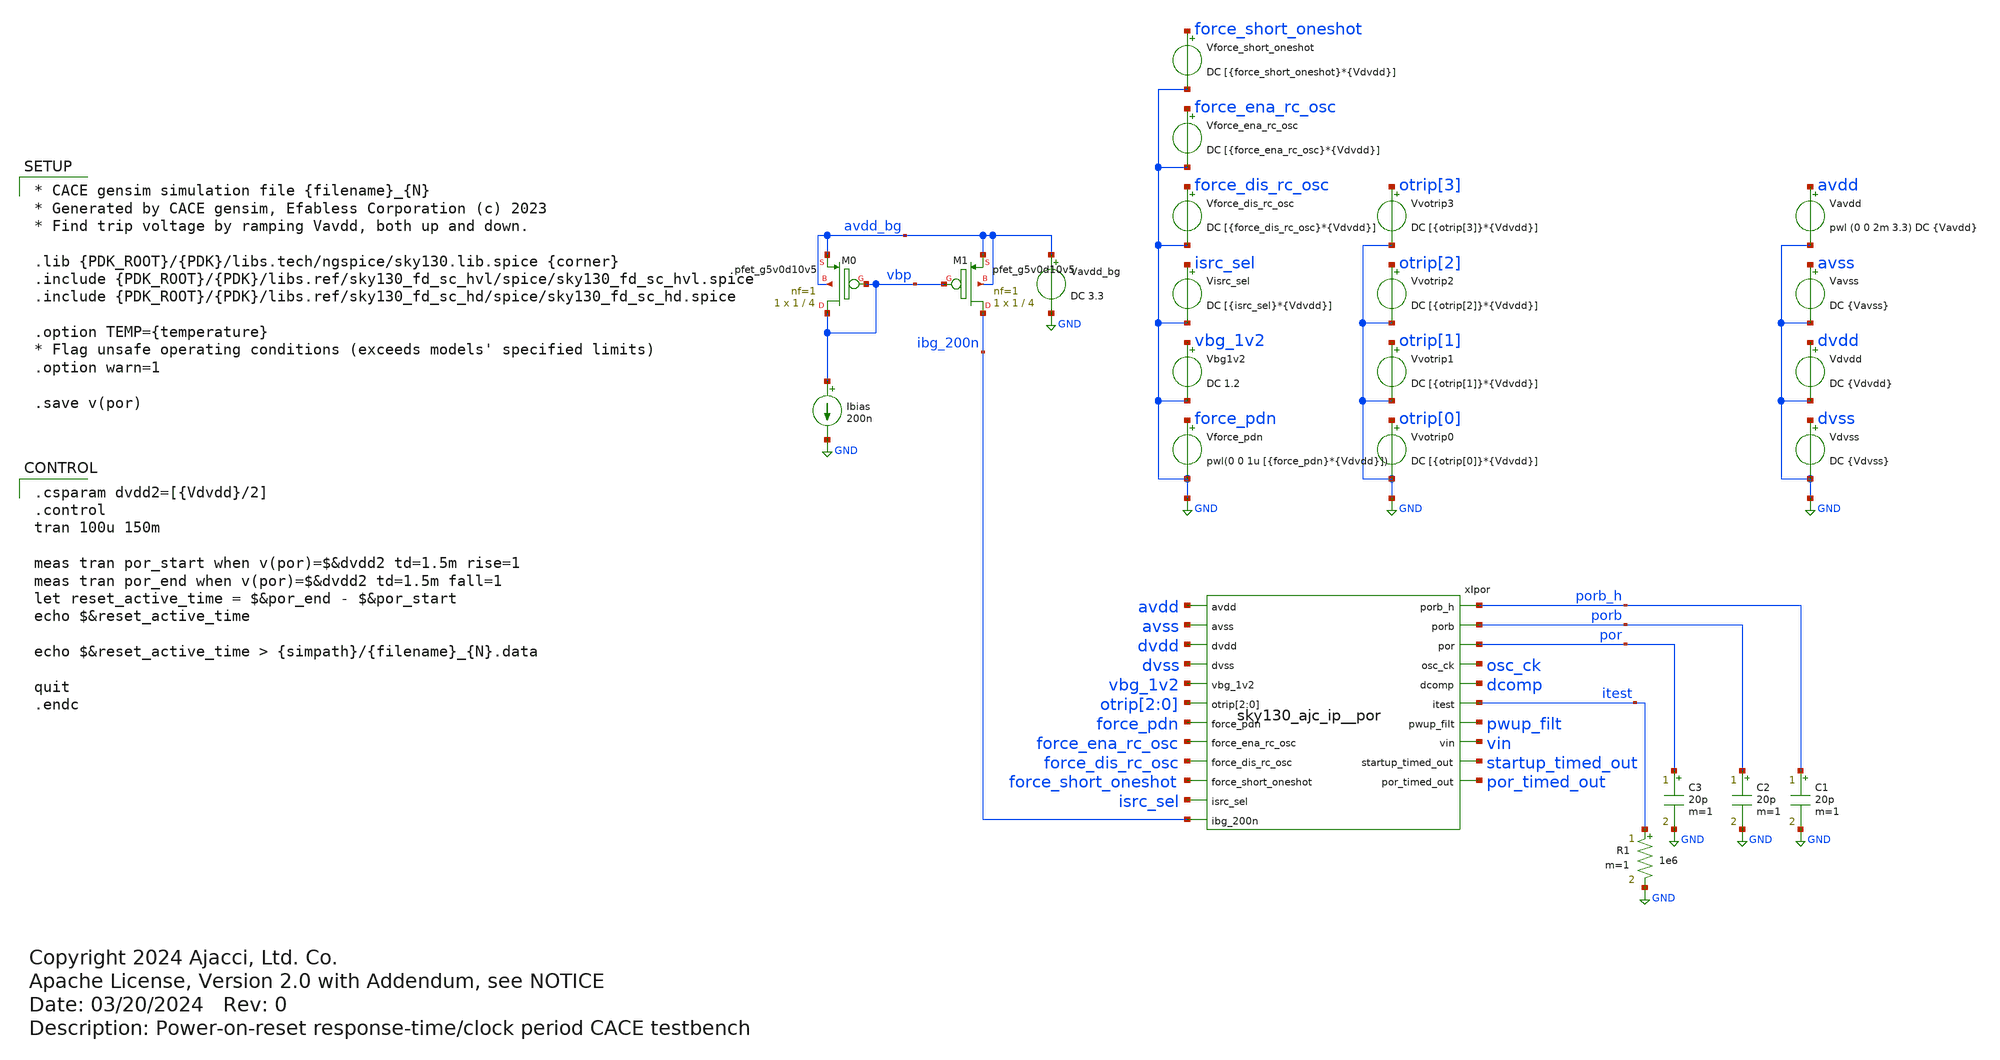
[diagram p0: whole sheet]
** sch_path: cace/transient_long.sch
* Copyright 2024 Ajacci, Ltd. Co.
* Apache License, Version 2.0 with Addendum, see NOTICE
**.subckt transient_long
Ibias vbp GND 200n
XM1 ibg_200n vbp avdd_bg avdd_bg sky130_fd_pr__pfet_g5v0d10v5 L=4 W=1 nf=1 ad='int((nf+1)/2) * W/nf * 0.29'
+ as='int((nf+2)/2) * W/nf * 0.29' pd='2*int((nf+1)/2) * (W/nf + 0.29)' ps='2*int((nf+2)/2) * (W/nf + 0.29)'
+ nrd='0.29 / W' nrs='0.29 / W' sa=0 sb=0 sd=0 mult=1 m=1
XM0 vbp vbp avdd_bg avdd_bg sky130_fd_pr__pfet_g5v0d10v5 L=4 W=1 nf=1 ad='int((nf+1)/2) * W/nf * 0.29'
+ as='int((nf+2)/2) * W/nf * 0.29' pd='2*int((nf+1)/2) * (W/nf + 0.29)' ps='2*int((nf+2)/2) * (W/nf + 0.29)'
+ nrd='0.29 / W' nrs='0.29 / W' sa=0 sb=0 sd=0 mult=1 m=1
R1 itest GND 1e6 m=1
Vavss avss GND DC {Vavss}
Vforce_pdn force_pdn GND pwl(0 0 1u [{force_pdn}*{Vdvdd}])
Vavdd avdd GND pwl (0 0 2m 3.3) DC {Vavdd}
.save i(vavdd)
Vbg1v2 vbg_1v2 GND DC 1.2
Vdvss dvss GND DC {Vdvss}
Vdvdd dvdd GND DC {Vdvdd}
.save i(vdvdd)
Vvotrip0 otrip[0] GND DC [{otrip[0]}*{Vdvdd}]
.save i(vvotrip0)
Vvotrip1 otrip[1] GND DC [{otrip[1]}*{Vdvdd}]
.save i(vvotrip1)
Vvotrip2 otrip[2] GND DC [{otrip[2]}*{Vdvdd}]
.save i(vvotrip2)
Vvotrip3 otrip[3] GND DC [{otrip[3]}*{Vdvdd}]
.save i(vvotrip3)
Visrc_sel isrc_sel GND DC [{isrc_sel}*{Vdvdd}]
Vavdd_bg avdd_bg GND DC 3.3
Vforce_dis_rc_osc force_dis_rc_osc GND DC [{force_dis_rc_osc}*{Vdvdd}]
Vforce_short_oneshot force_short_oneshot GND DC [{force_short_oneshot}*{Vdvdd}]
Vforce_ena_rc_osc force_ena_rc_osc GND DC [{force_ena_rc_osc}*{Vdvdd}]
xIpor avdd porb_h porb avss dvdd por dvss osc_ck vbg_1v2 dcomp otrip[2] otrip[1] otrip[0] itest
+ force_pdn pwup_filt vin force_ena_rc_osc force_dis_rc_osc startup_timed_out por_timed_out force_short_oneshot
+ isrc_sel ibg_200n sky130_ajc_ip__por
C1 porb_h GND 20p m=1
C2 porb GND 20p m=1
C3 por GND 20p m=1
**** begin user architecture code

* CACE gensim simulation file {filename}_{N}
* Generated by CACE gensim, Efabless Corporation (c) 2023
* Find trip voltage by ramping Vavdd, both up and down.

.lib {PDK_ROOT}/{PDK}/libs.tech/ngspice/sky130.lib.spice {corner}
.include {PDK_ROOT}/{PDK}/libs.ref/sky130_fd_sc_hvl/spice/sky130_fd_sc_hvl.spice
.include {PDK_ROOT}/{PDK}/libs.ref/sky130_fd_sc_hd/spice/sky130_fd_sc_hd.spice

.option TEMP={temperature}
* Flag unsafe operating conditions (exceeds models' specified limits)
.option warn=1

.save v(por)



.csparam dvdd2=[{Vdvdd}/2]
.control
tran 100u 150m

meas tran por_start when v(por)=$&dvdd2 td=1.5m rise=1
meas tran por_end when v(por)=$&dvdd2 td=1.5m fall=1
let reset_active_time = $&por_end - $&por_start
echo $&reset_active_time

echo $&reset_active_time > {simpath}/{filename}_{N}.data

quit
.endc


**** end user architecture code
**.ends
.GLOBAL GND
.end
